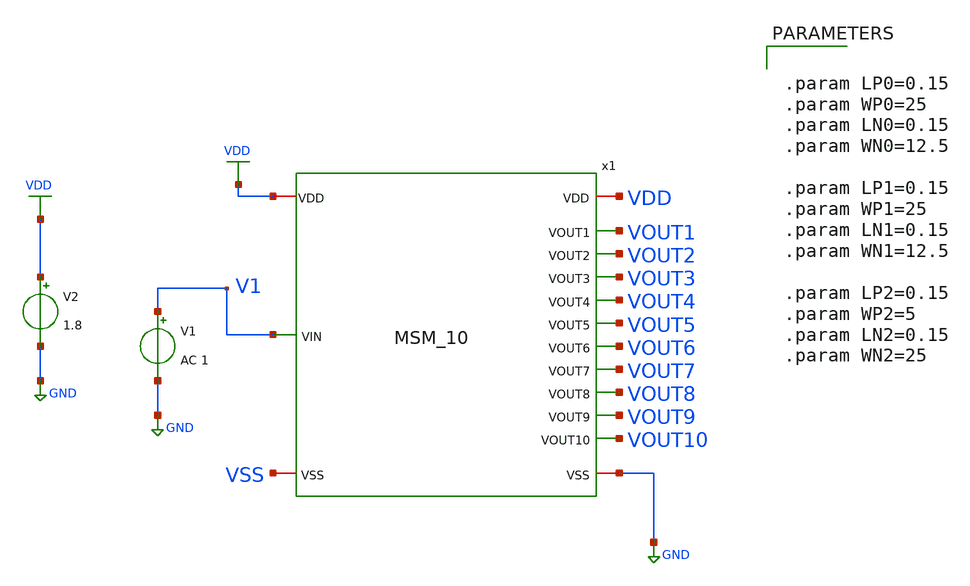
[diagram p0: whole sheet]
** sch_path: LIQAF circuit/10-Stage/Pre-Layout Simulations/DC Sweep.sch
**.subckt DC Sweep
V1 V1 GND AC 1
V2 VDD GND 1.8
x1 VDD VOUT1 VOUT2 V1 VOUT3 VOUT4 VOUT5 VOUT6 VOUT7 VOUT8 VOUT9 VOUT10 GND MSM_10
**** begin user architecture code
 ** manual skywater pdks install (with patches applied)
* .lib $::SKYWATER_MODELS/models/sky130.lib.spice tt

** opencircuitdesign pdks install
.lib $::SKYWATER_MODELS/sky130.lib.spice tt

.param mc_mm_switch=0
.param mc_pr_switch=0


.dc V1 0 1.8 0.01
.control
run
plot v(V1) v(VOUT1) v(VOUT2) v(VOUT3) v(VOUT4) v(VOUT5) v(VOUT6) v(VOUT7) v(VOUT8) v(VOUT9)
+ v(VOUT10)
.endc
.save all



.param LP0=0.15
.param WP0=25
.param LN0=0.15
.param WN0=12.5

.param LP1=0.15
.param WP1=25
.param LN1=0.15
.param WN1=12.5

.param LP2=0.15
.param WP2=5
.param LN2=0.15
.param WN2=25


**** end user architecture code
**.ends
.GLOBAL GND
.GLOBAL VDD
.end
